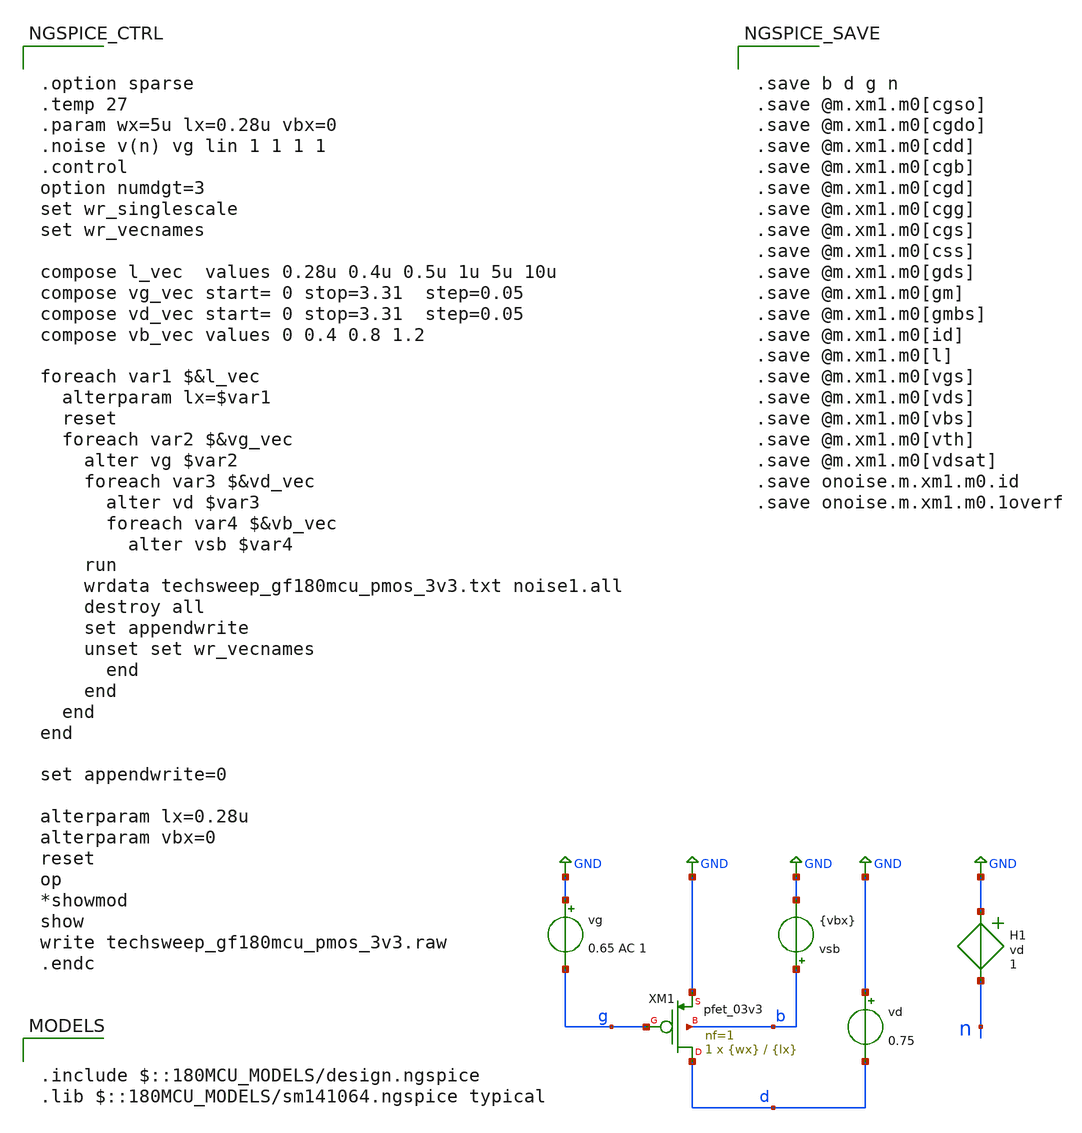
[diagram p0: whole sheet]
** sch_path: designs/Sizing/techsweep_gf180mcu_pmos_3v3.sch
* (c) 2025 H. Pretl, Apache-2.0 license
**.subckt techsweep_gf180mcu_pmos_3v3
vd GND d 0.75
vsb b GND {vbx}
vg GND g 0.65 AC 1
H1 GND n vd 1
XM1 d g GND b pfet_03v3 L={lx} W={wx} nf=1 ad='int((nf+1)/2) * W/nf * 0.18u' as='int((nf+2)/2) * W/nf * 0.18u'
+ pd='2*int((nf+1)/2) * (W/nf + 0.18u)' ps='2*int((nf+2)/2) * (W/nf + 0.18u)' nrd='0.18u / W' nrs='0.18u / W'
+ sa=0 sb=0 sd=0 m=1
**** begin user architecture code


.option sparse
.temp 27
.param wx=5u lx=0.28u vbx=0
.noise v(n) vg lin 1 1 1 1
.control
option numdgt=3
set wr_singlescale
set wr_vecnames

compose l_vec  values 0.28u 0.4u 0.5u 1u 5u 10u
compose vg_vec start= 0 stop=3.31  step=0.05
compose vd_vec start= 0 stop=3.31  step=0.05
compose vb_vec values 0 0.4 0.8 1.2

foreach var1 $&l_vec
  alterparam lx=$var1
  reset
  foreach var2 $&vg_vec
    alter vg $var2
    foreach var3 $&vd_vec
      alter vd $var3
      foreach var4 $&vb_vec
        alter vsb $var4
	run
	wrdata techsweep_gf180mcu_pmos_3v3.txt noise1.all
	destroy all
	set appendwrite
	unset set wr_vecnames
      end
    end
  end
end

set appendwrite=0

alterparam lx=0.28u
alterparam vbx=0
reset
op
*showmod
show
write techsweep_gf180mcu_pmos_3v3.raw
.endc




.save b d g n
.save @m.xm1.m0[cgso]
.save @m.xm1.m0[cgdo]
.save @m.xm1.m0[cdd]
.save @m.xm1.m0[cgb]
.save @m.xm1.m0[cgd]
.save @m.xm1.m0[cgg]
.save @m.xm1.m0[cgs]
.save @m.xm1.m0[css]
.save @m.xm1.m0[gds]
.save @m.xm1.m0[gm]
.save @m.xm1.m0[gmbs]
.save @m.xm1.m0[id]
.save @m.xm1.m0[l]
.save @m.xm1.m0[vgs]
.save @m.xm1.m0[vds]
.save @m.xm1.m0[vbs]
.save @m.xm1.m0[vth]
.save @m.xm1.m0[vdsat]
.save onoise.m.xm1.m0.id
.save onoise.m.xm1.m0.1overf



.include $::180MCU_MODELS/design.ngspice
.lib $::180MCU_MODELS/sm141064.ngspice typical

**** end user architecture code
**.ends
.GLOBAL GND
.end
